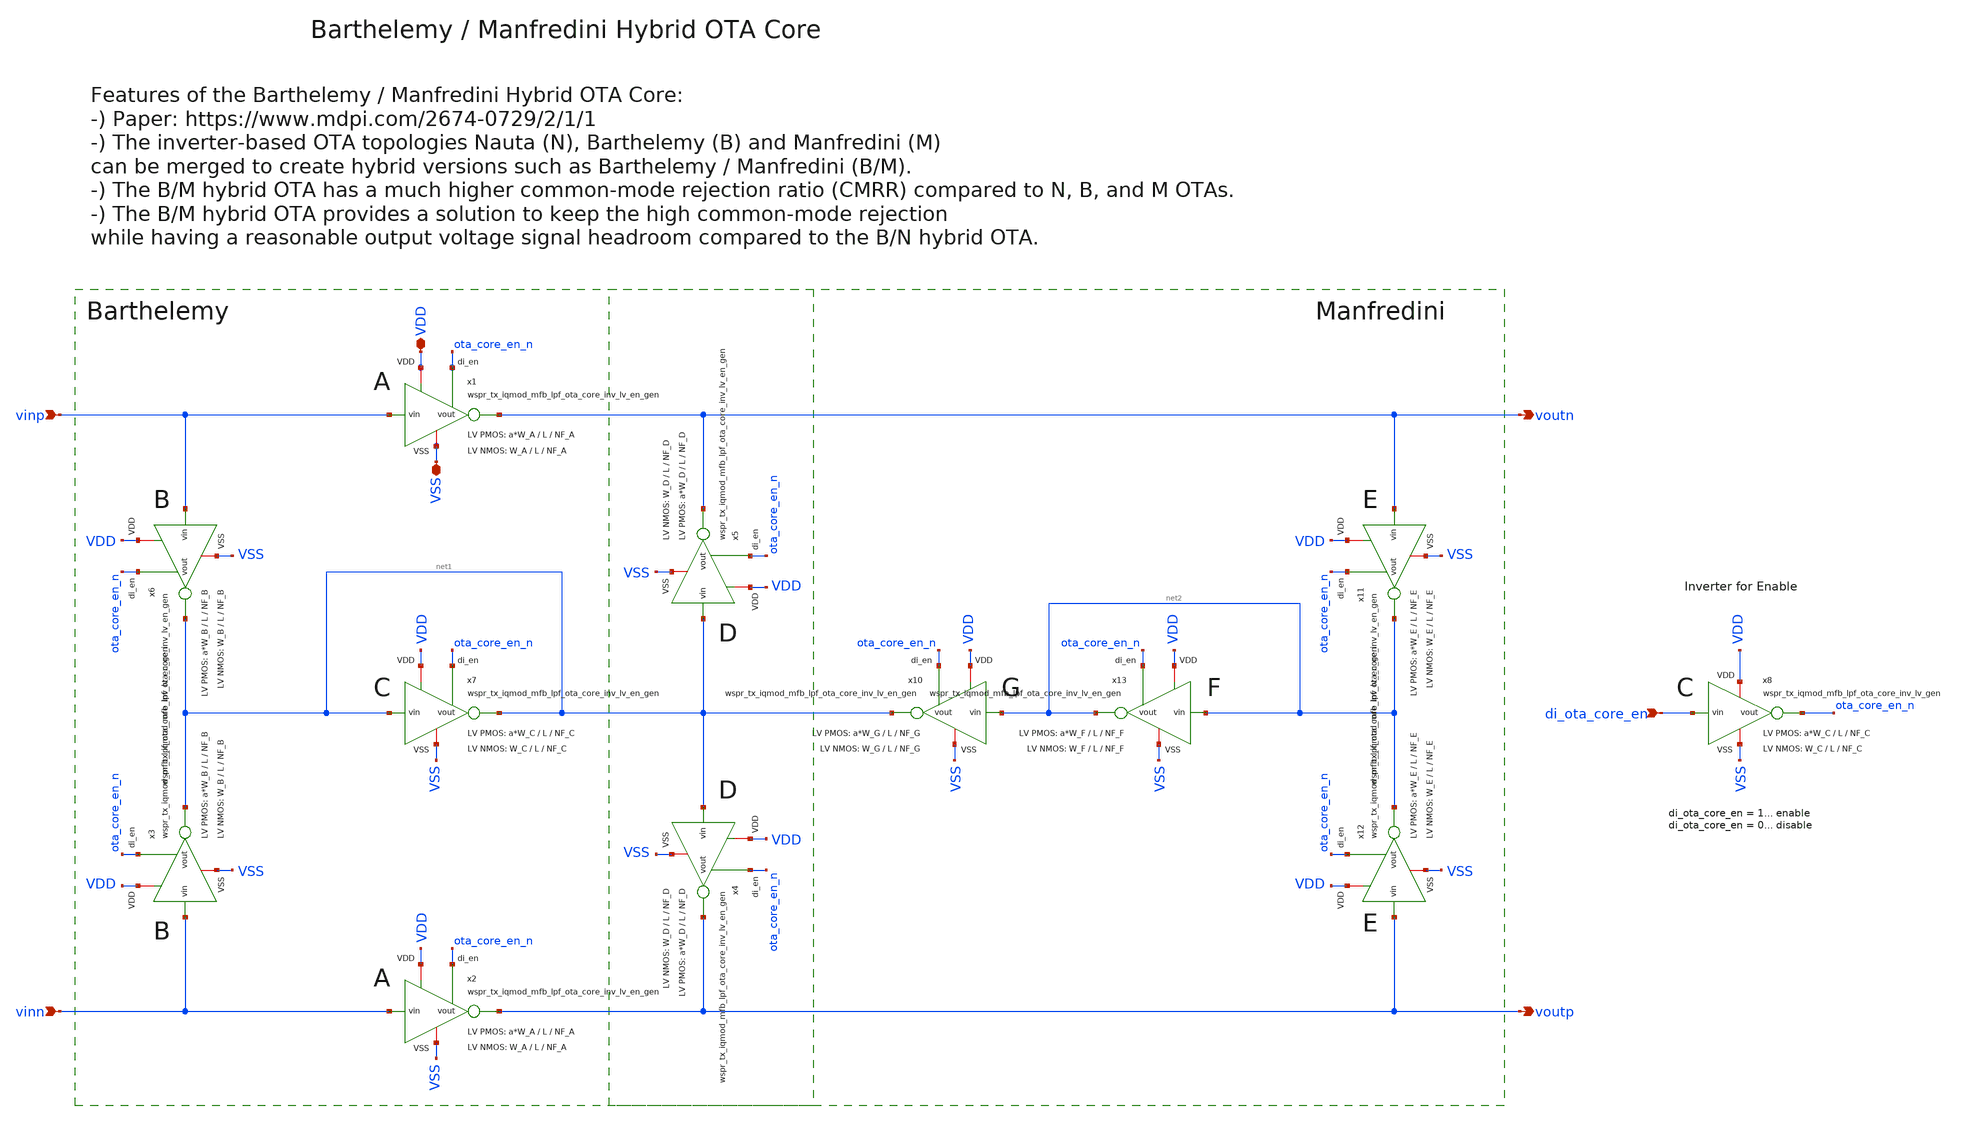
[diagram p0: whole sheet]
** sch_path: sky130/xschem/generic/wspr_tx_iqmod_mfb_lpf_ota_core_hybrid_bm_gen.sch
**.subckt wspr_tx_iqmod_mfb_lpf_ota_core_hybrid_bm_gen di_ota_core_en vinp vinn VDD VSS voutp voutn
*.ipin di_ota_core_en
*.ipin vinp
*.ipin vinn
*.iopin VDD
*.iopin VSS
*.opin voutp
*.opin voutn
x2 VDD vinn voutp VSS ota_core_en_n wspr_tx_iqmod_mfb_lpf_ota_core_inv_lv_en_gen W_P=a*W_A L_P=L
+ NF_P=NF_A W_N=W_A L_N=L NF_N=NF_A
x1 VDD vinp voutn VSS ota_core_en_n wspr_tx_iqmod_mfb_lpf_ota_core_inv_lv_en_gen W_P=a*W_A L_P=L
+ NF_P=NF_A W_N=W_A L_N=L NF_N=NF_A
x4 VDD net1 voutp VSS ota_core_en_n wspr_tx_iqmod_mfb_lpf_ota_core_inv_lv_en_gen W_P=a*W_D L_P=L
+ NF_P=NF_D W_N=W_D L_N=L NF_N=NF_D
x5 VDD net1 voutn VSS ota_core_en_n wspr_tx_iqmod_mfb_lpf_ota_core_inv_lv_en_gen W_P=a*W_D L_P=L
+ NF_P=NF_D W_N=W_D L_N=L NF_N=NF_D
x6 VDD vinp net1 VSS ota_core_en_n wspr_tx_iqmod_mfb_lpf_ota_core_inv_lv_en_gen W_P=a*W_B L_P=L
+ NF_P=NF_B W_N=W_B L_N=L NF_N=NF_B
x3 VDD vinn net1 VSS ota_core_en_n wspr_tx_iqmod_mfb_lpf_ota_core_inv_lv_en_gen W_P=a*W_B L_P=L
+ NF_P=NF_B W_N=W_B L_N=L NF_N=NF_B
x7 VDD net1 net1 VSS ota_core_en_n wspr_tx_iqmod_mfb_lpf_ota_core_inv_lv_en_gen W_P=a*W_C L_P=L
+ NF_P=NF_C W_N=W_C L_N=L NF_N=NF_C
x8 VDD di_ota_core_en ota_core_en_n VSS wspr_tx_iqmod_mfb_lpf_ota_core_inv_lv_gen W_P=a*W_C L_P=L
+ NF_P=NF_C W_N=W_C L_N=L NF_N=NF_C
x10 VDD net2 net1 VSS ota_core_en_n wspr_tx_iqmod_mfb_lpf_ota_core_inv_lv_en_gen W_P=a*W_G L_P=L
+ NF_P=NF_G W_N=W_G L_N=L NF_N=NF_G
x11 VDD voutn net2 VSS ota_core_en_n wspr_tx_iqmod_mfb_lpf_ota_core_inv_lv_en_gen W_P=a*W_E L_P=L
+ NF_P=NF_E W_N=W_E L_N=L NF_N=NF_E
x12 VDD voutp net2 VSS ota_core_en_n wspr_tx_iqmod_mfb_lpf_ota_core_inv_lv_en_gen W_P=a*W_E L_P=L
+ NF_P=NF_E W_N=W_E L_N=L NF_N=NF_E
x13 VDD net2 net2 VSS ota_core_en_n wspr_tx_iqmod_mfb_lpf_ota_core_inv_lv_en_gen W_P=a*W_F L_P=L
+ NF_P=NF_F W_N=W_F L_N=L NF_N=NF_F
**.ends
.end
